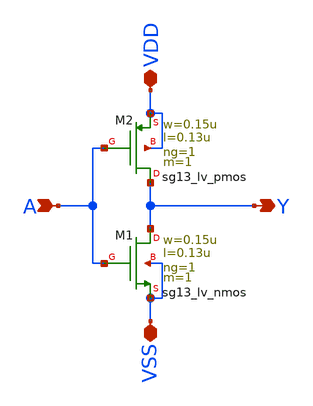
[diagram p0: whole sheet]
** sch_path: test-schematics/ihp/inv.sch
**.subckt inv VDD A Y VSS
*.iopin VDD
*.ipin A
*.opin Y
*.iopin VSS
XM1 Y A VSS VSS sg13_lv_nmos w=0.15u l=0.13u ng=1 m=1 mm_ok=1
XM2 Y A VDD VDD sg13_lv_pmos w=0.15u l=0.13u ng=1 m=1 mm_ok=1
**.ends
.end
